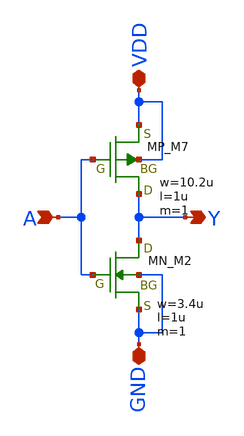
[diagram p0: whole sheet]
** sch_path: libs.tech/xschem/TR-1um_5_stdcell/INV_X1.sch
**.subckt INV_X1 A Y GND VDD
*.ipin A
*.opin Y
*.iopin GND
*.iopin VDD
XM7 Y A VDD VDD PMOS w=10.2u l=1u nrd=0 nrs=0 m=1
XM2 Y A GND GND NMOS w=3.4u l=1u nrd=0 nrs=0 m=1
**.ends
.end
